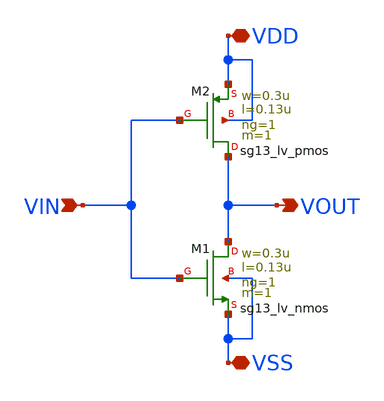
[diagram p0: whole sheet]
** sch_path: ADC8711-main/schematic/xschem/INV_D2.sch
**.subckt INV_D2 VDD VSS VOUT VIN
*.iopin VDD
*.iopin VSS
*.opin VOUT
*.ipin VIN
XM1 VOUT VIN VSS VSS sg13_lv_nmos w=0.3u l=0.13u ng=1 m=1 mm_ok=1
XM2 VOUT VIN VDD VDD sg13_lv_pmos w=0.3u l=0.13u ng=1 m=1 mm_ok=1
**.ends
.end
